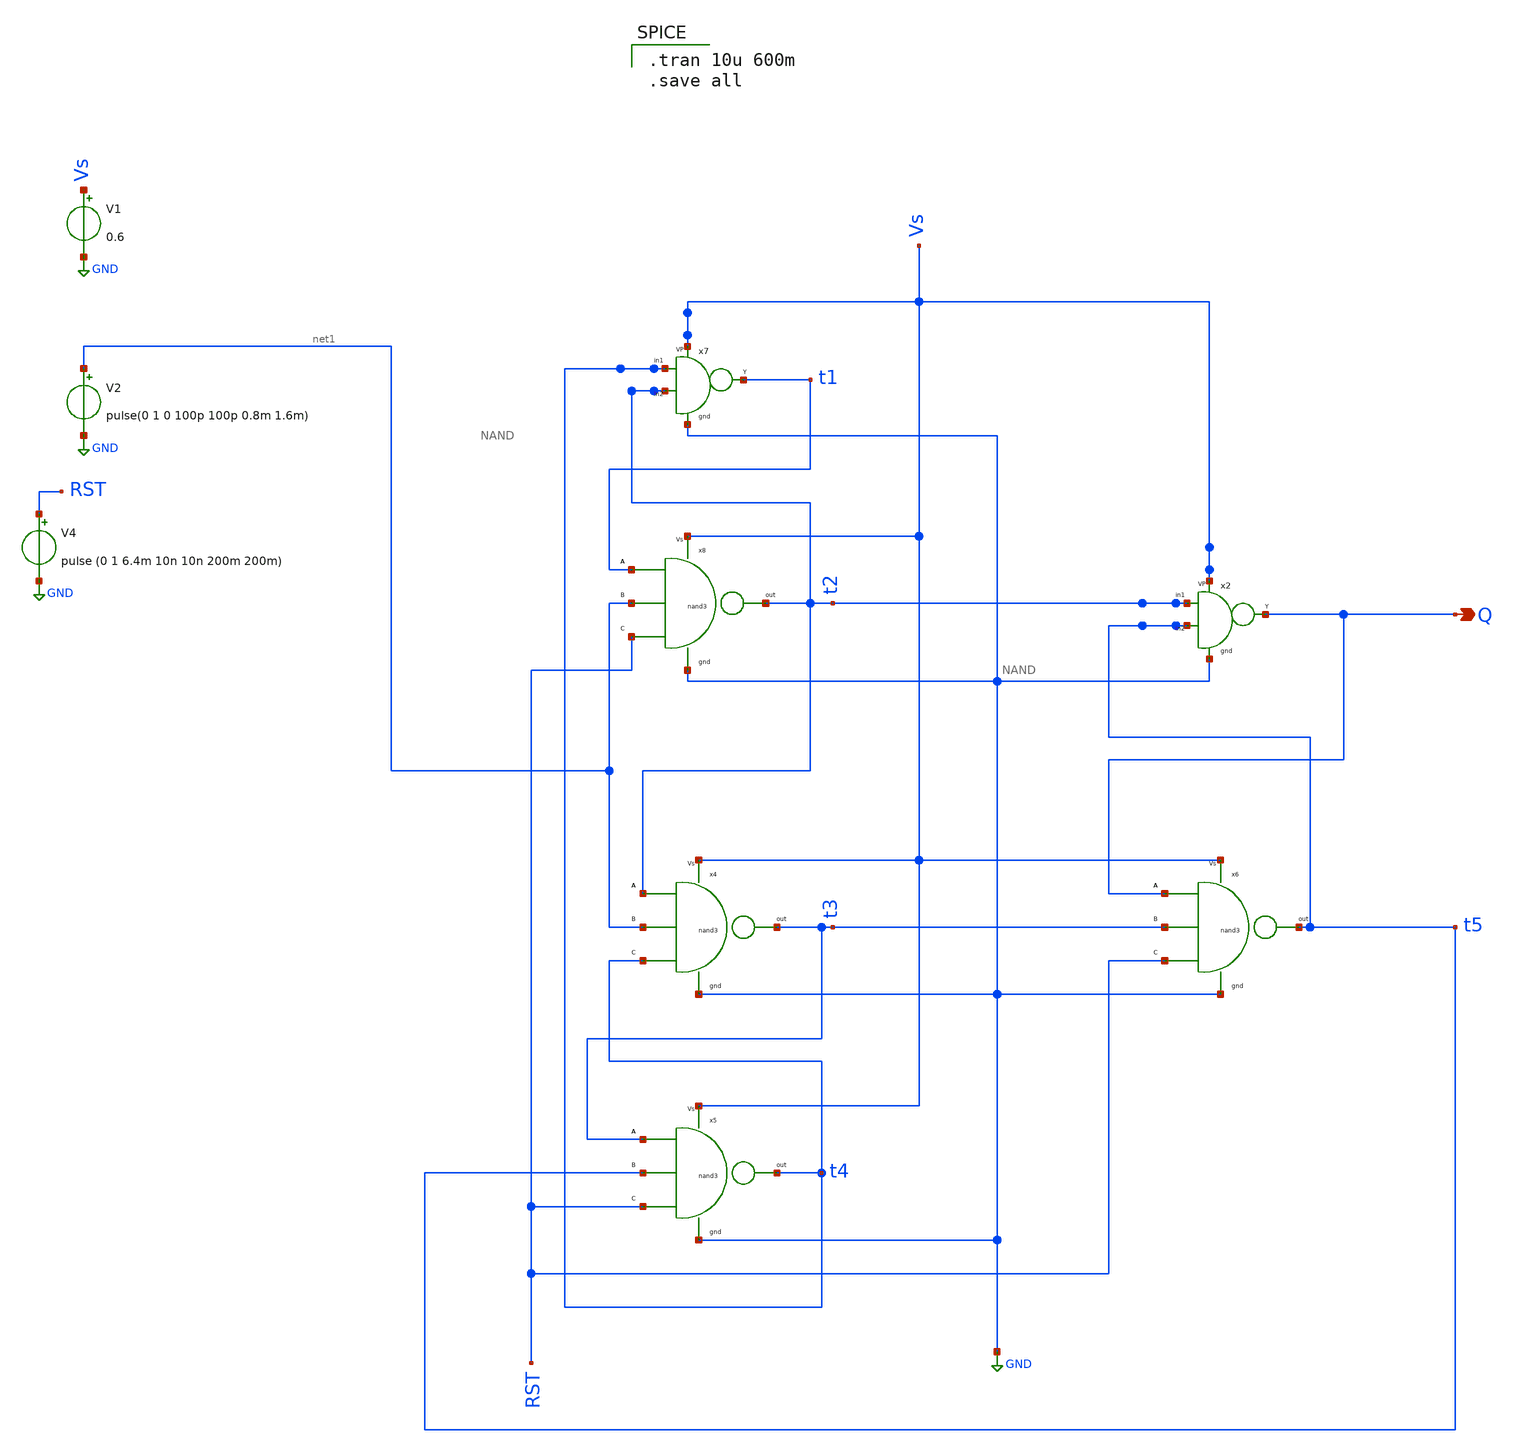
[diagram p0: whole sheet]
** sch_path: untitled-3.sch
**.subckt untitled-3 Q
*.opin Q
V1 Vs GND 0.6
V2 net1 GND pulse(0 1 0 100p 100p 0.8m 1.6m)
V4 RST GND pulse (0 1 6.4m 10n 10n 200m 200m)
x7 t2 t4 t1 Vs GND NAND
x8 t1 net1 RST Vs GND t2 NAND3
x6 Q t3 RST Vs GND t5 NAND3
x4 t2 net1 t4 Vs GND t3 NAND3
x5 t3 t5 RST Vs GND t4 NAND3
x2 t5 t2 Q Vs GND NAND
**** begin user architecture code

** opencircuitdesign pdks install
.lib $::SKYWATER_MODELS/sky130.lib.spice tt



.tran 10u 600m
.save all

**** end user architecture code
**.ends

* expanding   symbol:  component/NAND2/NAND.sym # of pins=5
** sym_path: component/NAND2/NAND.sym
** sch_path: component/NAND2/NAND.sch
.subckt NAND B A Y VP VN
*.iopin VP
*.ipin A
*.ipin B
*.opin Y
*.iopin VN
XM1 Y A VP VP sky130_fd_pr__pfet_01v8 L=0.15 W=1.26 nf=1 ad='int((nf+1)/2) * W/nf * 0.29' as='int((nf+2)/2) * W/nf * 0.29'
+ pd='2*int((nf+1)/2) * (W/nf + 0.29)' ps='2*int((nf+2)/2) * (W/nf + 0.29)' nrd='0.29 / W' nrs='0.29 / W'
+ sa=0 sb=0 sd=0 mult=1 m=1
XM2 Y B VP VP sky130_fd_pr__pfet_01v8 L=0.15 W=1.26 nf=1 ad='int((nf+1)/2) * W/nf * 0.29' as='int((nf+2)/2) * W/nf * 0.29'
+ pd='2*int((nf+1)/2) * (W/nf + 0.29)' ps='2*int((nf+2)/2) * (W/nf + 0.29)' nrd='0.29 / W' nrs='0.29 / W'
+ sa=0 sb=0 sd=0 mult=1 m=1
XM3 Y A net1 net1 sky130_fd_pr__nfet_01v8 L=0.15 W=0.84 nf=1 ad='int((nf+1)/2) * W/nf * 0.29' as='int((nf+2)/2) * W/nf * 0.29'
+ pd='2*int((nf+1)/2) * (W/nf + 0.29)' ps='2*int((nf+2)/2) * (W/nf + 0.29)' nrd='0.29 / W' nrs='0.29 / W'
+ sa=0 sb=0 sd=0 mult=1 m=1
XM4 net1 B VN VN sky130_fd_pr__nfet_01v8 L=0.15 W=0.84 nf=1 ad='int((nf+1)/2) * W/nf * 0.29' as='int((nf+2)/2) * W/nf * 0.29'
+ pd='2*int((nf+1)/2) * (W/nf + 0.29)' ps='2*int((nf+2)/2) * (W/nf + 0.29)' nrd='0.29 / W' nrs='0.29 / W'
+ sa=0 sb=0 sd=0 mult=1 m=1
.ends


* expanding   symbol:  component/NAND3/NAND3.sym # of pins=6
** sym_path: component/NAND3/NAND3.sym
** sch_path: component/NAND3/NAND3.sch
.subckt NAND3 A B C VP VN Y
*.iopin VP
*.iopin VN
*.ipin A
*.ipin B
*.ipin C
*.opin Y
XM1 Y A net1 VN sky130_fd_pr__nfet_01v8 L=0.15 W=1.26 nf=1 ad='int((nf+1)/2) * W/nf * 0.29' as='int((nf+2)/2) * W/nf * 0.29'
+ pd='2*int((nf+1)/2) * (W/nf + 0.29)' ps='2*int((nf+2)/2) * (W/nf + 0.29)' nrd='0.29 / W' nrs='0.29 / W'
+ sa=0 sb=0 sd=0 mult=1 m=1
XM2 net1 B net2 VN sky130_fd_pr__nfet_01v8 L=0.15 W=1.26 nf=1 ad='int((nf+1)/2) * W/nf * 0.29' as='int((nf+2)/2) * W/nf * 0.29'
+ pd='2*int((nf+1)/2) * (W/nf + 0.29)' ps='2*int((nf+2)/2) * (W/nf + 0.29)' nrd='0.29 / W' nrs='0.29 / W'
+ sa=0 sb=0 sd=0 mult=1 m=1
XM3 net2 C VN VN sky130_fd_pr__nfet_01v8 L=0.15 W=1.26 nf=1 ad='int((nf+1)/2) * W/nf * 0.29' as='int((nf+2)/2) * W/nf * 0.29'
+ pd='2*int((nf+1)/2) * (W/nf + 0.29)' ps='2*int((nf+2)/2) * (W/nf + 0.29)' nrd='0.29 / W' nrs='0.29 / W'
+ sa=0 sb=0 sd=0 mult=1 m=1
XM4 Y A VP VP sky130_fd_pr__pfet_01v8 L=0.15 W=1.26 nf=1 ad='int((nf+1)/2) * W/nf * 0.29' as='int((nf+2)/2) * W/nf * 0.29'
+ pd='2*int((nf+1)/2) * (W/nf + 0.29)' ps='2*int((nf+2)/2) * (W/nf + 0.29)' nrd='0.29 / W' nrs='0.29 / W'
+ sa=0 sb=0 sd=0 mult=1 m=1
XM5 Y B VP VP sky130_fd_pr__pfet_01v8 L=0.15 W=1.26 nf=1 ad='int((nf+1)/2) * W/nf * 0.29' as='int((nf+2)/2) * W/nf * 0.29'
+ pd='2*int((nf+1)/2) * (W/nf + 0.29)' ps='2*int((nf+2)/2) * (W/nf + 0.29)' nrd='0.29 / W' nrs='0.29 / W'
+ sa=0 sb=0 sd=0 mult=1 m=1
XM6 Y C VP VP sky130_fd_pr__pfet_01v8 L=0.15 W=1.26 nf=1 ad='int((nf+1)/2) * W/nf * 0.29' as='int((nf+2)/2) * W/nf * 0.29'
+ pd='2*int((nf+1)/2) * (W/nf + 0.29)' ps='2*int((nf+2)/2) * (W/nf + 0.29)' nrd='0.29 / W' nrs='0.29 / W'
+ sa=0 sb=0 sd=0 mult=1 m=1
.ends

.GLOBAL GND
.end
